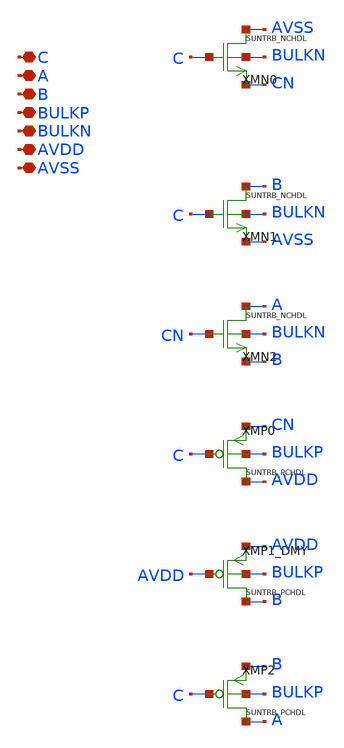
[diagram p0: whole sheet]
** sch_path: design/SUN_TRB_SKY130NM/SUNTRB_TGPD_CV.sch
**.subckt SUNTRB_TGPD_CV C A B BULKP BULKN AVDD AVSS
*.iopin C
*.iopin A
*.iopin B
*.iopin BULKP
*.iopin BULKN
*.iopin AVDD
*.iopin AVSS
XMN0 AVSS C CN BULKN SUNTRB_NCHDL xoffset=0 yoffset=0 angle=0
XMN1 B C AVSS BULKN SUNTRB_NCHDL xoffset=0 yoffset=0 angle=0
XMN2 A CN B BULKN SUNTRB_NCHDL xoffset=0 yoffset=0 angle=0
XMP0 AVDD C CN BULKP SUNTRB_PCHDL xoffset=0 yoffset=0 angle=0 M=1
XMP1_DMY B AVDD AVDD BULKP SUNTRB_PCHDL xoffset=0 yoffset=0 angle=0 M=1
XMP2 A C B BULKP SUNTRB_PCHDL xoffset=0 yoffset=0 angle=0 M=1
**.ends
.end
